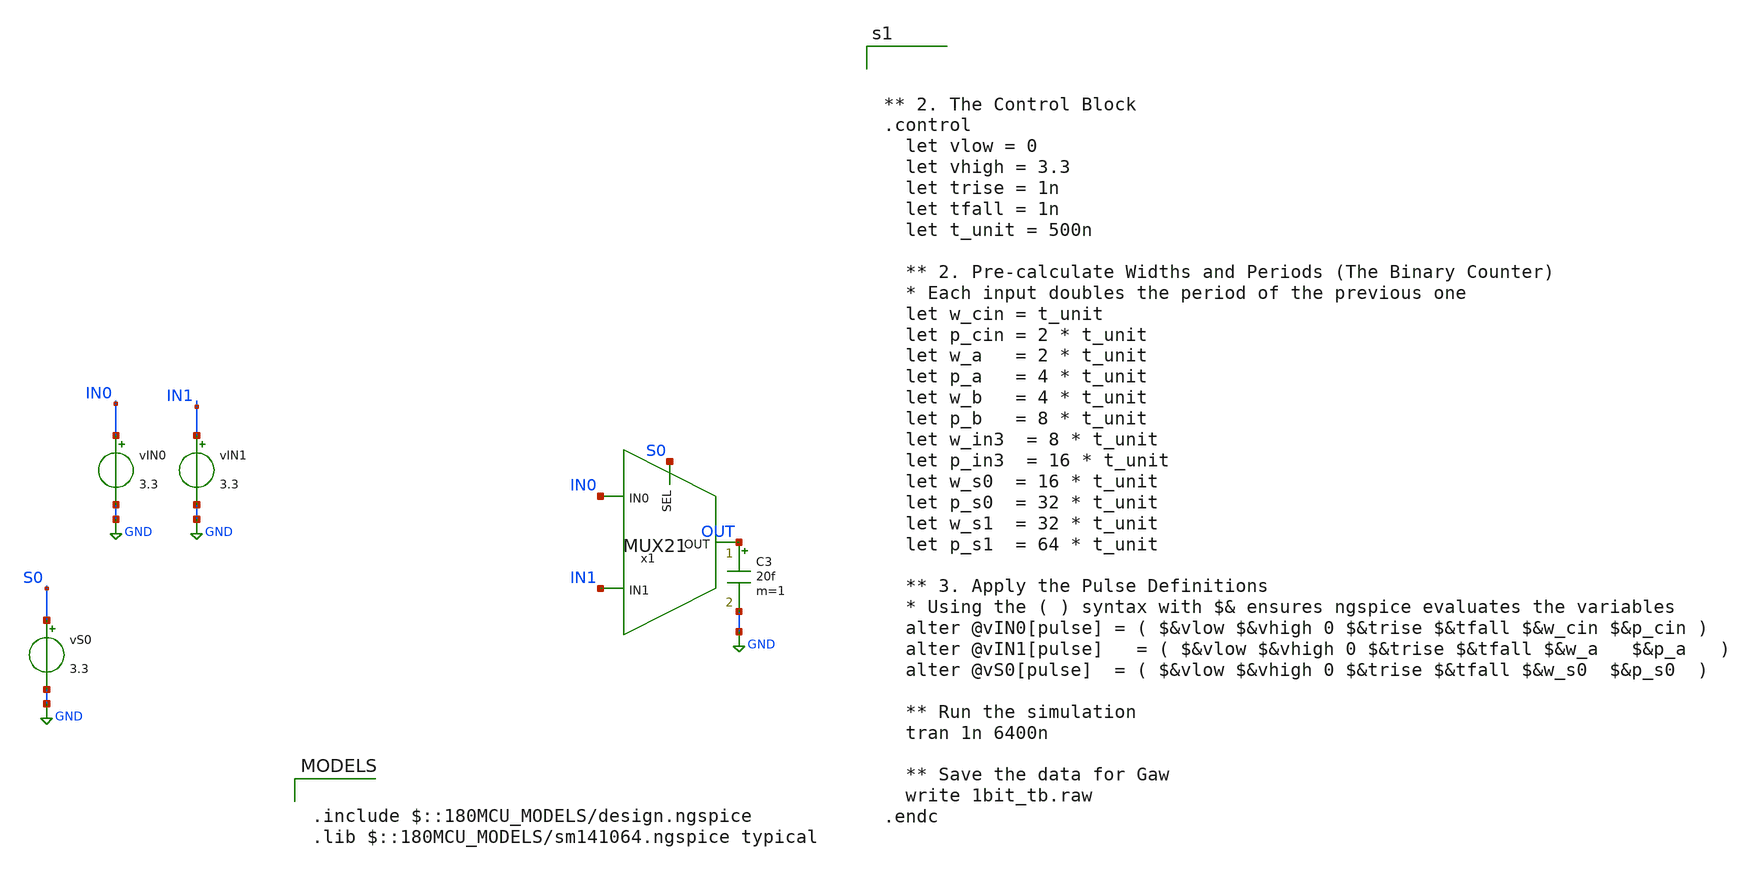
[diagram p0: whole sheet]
** sch_path: tbs/mux21_tb.sch
**.subckt mux21_tb
vIN1 IN1 GND 3.3
vIN0 IN0 GND 3.3
vS0 S0 GND 3.3
C3 OUT GND 20f m=1
x1 IN0 S0 OUT IN1 MUX21
**** begin user architecture code

.include $::180MCU_MODELS/design.ngspice
.lib $::180MCU_MODELS/sm141064.ngspice typical




** 2. The Control Block
.control
  let vlow = 0
  let vhigh = 3.3
  let trise = 1n
  let tfall = 1n
  let t_unit = 500n

  ** 2. Pre-calculate Widths and Periods (The Binary Counter)
  * Each input doubles the period of the previous one
  let w_cin = t_unit
  let p_cin = 2 * t_unit
  let w_a   = 2 * t_unit
  let p_a   = 4 * t_unit
  let w_b   = 4 * t_unit
  let p_b   = 8 * t_unit
  let w_in3  = 8 * t_unit
  let p_in3  = 16 * t_unit
  let w_s0  = 16 * t_unit
  let p_s0  = 32 * t_unit
  let w_s1  = 32 * t_unit
  let p_s1  = 64 * t_unit

  ** 3. Apply the Pulse Definitions
  * Using the ( ) syntax with $& ensures ngspice evaluates the variables
  alter @vIN0[pulse] = ( $&vlow $&vhigh 0 $&trise $&tfall $&w_cin $&p_cin )
  alter @vIN1[pulse]   = ( $&vlow $&vhigh 0 $&trise $&tfall $&w_a   $&p_a   )
  alter @vS0[pulse]  = ( $&vlow $&vhigh 0 $&trise $&tfall $&w_s0  $&p_s0  )

  ** Run the simulation
  tran 1n 6400n

  ** Save the data for Gaw
  write 1bit_tb.raw
.endc


**** end user architecture code
**.ends
.GLOBAL GND
.end
